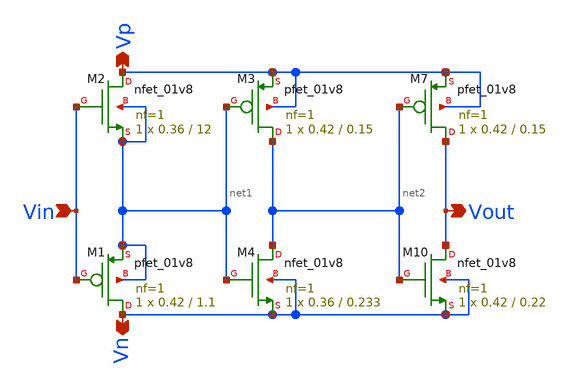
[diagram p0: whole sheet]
** sch_path: xschem/Vth_sch/Symbol/th01.sch
**.subckt th01 Vn Vp Vin Vout
*.opin Vn
*.opin Vp
*.ipin Vin
*.opin Vout
XM1 Vn Vin net1 net1 sky130_fd_pr__pfet_01v8 L=1.1 W=0.42 nf=1 ad='int((nf+1)/2) * W/nf * 0.29' as='int((nf+2)/2) * W/nf * 0.29'
+ pd='2*int((nf+1)/2) * (W/nf + 0.29)' ps='2*int((nf+2)/2) * (W/nf + 0.29)' nrd='0.29 / W' nrs='0.29 / W'
+ sa=0 sb=0 sd=0 mult=1 m=1
XM2 Vp Vin net1 net1 sky130_fd_pr__nfet_01v8 L=12 W=0.36 nf=1 ad='int((nf+1)/2) * W/nf * 0.29' as='int((nf+2)/2) * W/nf * 0.29'
+ pd='2*int((nf+1)/2) * (W/nf + 0.29)' ps='2*int((nf+2)/2) * (W/nf + 0.29)' nrd='0.29 / W' nrs='0.29 / W'
+ sa=0 sb=0 sd=0 mult=1 m=1
XM7 Vout net2 Vp Vp sky130_fd_pr__pfet_01v8 L=0.15 W=0.42 nf=1 ad='int((nf+1)/2) * W/nf * 0.29' as='int((nf+2)/2) * W/nf * 0.29'
+ pd='2*int((nf+1)/2) * (W/nf + 0.29)' ps='2*int((nf+2)/2) * (W/nf + 0.29)' nrd='0.29 / W' nrs='0.29 / W'
+ sa=0 sb=0 sd=0 mult=1 m=1
XM10 Vout net2 Vn Vn sky130_fd_pr__nfet_01v8 L=0.22 W=0.42 nf=1 ad='int((nf+1)/2) * W/nf * 0.29' as='int((nf+2)/2) * W/nf * 0.29'
+ pd='2*int((nf+1)/2) * (W/nf + 0.29)' ps='2*int((nf+2)/2) * (W/nf + 0.29)' nrd='0.29 / W' nrs='0.29 / W'
+ sa=0 sb=0 sd=0 mult=1 m=1
XM3 net2 net1 Vp Vp sky130_fd_pr__pfet_01v8 L=0.15 W=0.42 nf=1 ad='int((nf+1)/2) * W/nf * 0.29' as='int((nf+2)/2) * W/nf * 0.29'
+ pd='2*int((nf+1)/2) * (W/nf + 0.29)' ps='2*int((nf+2)/2) * (W/nf + 0.29)' nrd='0.29 / W' nrs='0.29 / W'
+ sa=0 sb=0 sd=0 mult=1 m=1
XM4 net2 net1 Vn Vn sky130_fd_pr__nfet_01v8 L=0.233 W=0.36 nf=1 ad='int((nf+1)/2) * W/nf * 0.29' as='int((nf+2)/2) * W/nf * 0.29'
+ pd='2*int((nf+1)/2) * (W/nf + 0.29)' ps='2*int((nf+2)/2) * (W/nf + 0.29)' nrd='0.29 / W' nrs='0.29 / W'
+ sa=0 sb=0 sd=0 mult=1 m=1
**.ends
.end
